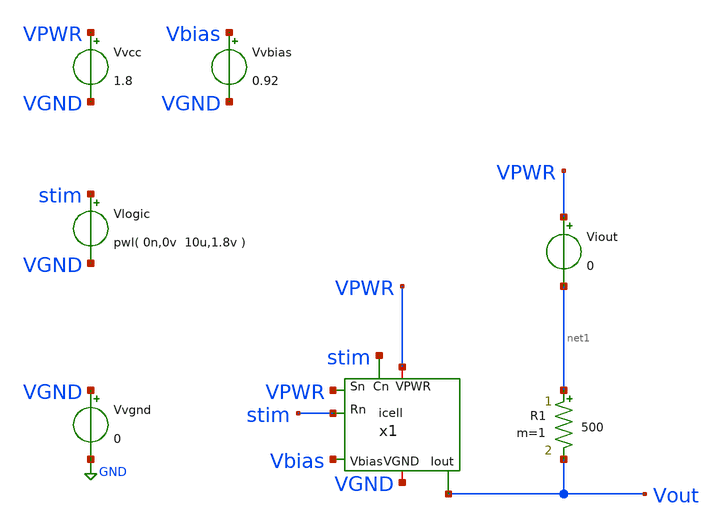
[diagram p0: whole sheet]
** sch_path: xschem/tb_icell.sch
**.subckt tb_icell
x1 VPWR VGND stim stim VPWR Vbias Vout icell
Vvcc VPWR VGND 1.8
R1 net1 Vout 500 m=1
Vvbias Vbias VGND 0.92
Vvgnd VGND GND 0
Viout VPWR net1 0
Vlogic stim VGND pwl( 0n,0v 10u,1.8v )
**** begin user architecture code



.options savecurrents
.control

    save all
    tran 1n 12.8u
    write tb_icell.raw vout

.endc




.lib $::SKYWATER_MODELS/sky130.lib.spice tt
.include $::SKYWATER_STDCELLS/sky130_fd_sc_hd.spice

**** end user architecture code
**.ends

* expanding   symbol:  icell.sym # of pins=7
** sym_path: xschem/icell.sym
** sch_path: xschem/icell.sch
.subckt icell VPWR VGND Rn Cn Sn Vbias Iout
*.ipin Rn
*.iopin VPWR
*.opin Iout
*.iopin VGND
*.ipin Cn
*.ipin Sn
*.ipin Vbias
XM2 net1 Sn VPWR VPWR sky130_fd_pr__pfet_01v8 L=0.15 W=0.5 nf=1 ad='int((nf+1)/2) * W/nf * 0.29' as='int((nf+2)/2) * W/nf * 0.29'
+ pd='2*int((nf+1)/2) * (W/nf + 0.29)' ps='2*int((nf+2)/2) * (W/nf + 0.29)' nrd='0.29 / W' nrs='0.29 / W'
+ sa=0 sb=0 sd=0 mult=1 m=1
XM3 net1 Sn net3 VGND sky130_fd_pr__nfet_01v8 L=0.15 W=0.5 nf=1 ad='int((nf+1)/2) * W/nf * 0.29' as='int((nf+2)/2) * W/nf * 0.29'
+ pd='2*int((nf+1)/2) * (W/nf + 0.29)' ps='2*int((nf+2)/2) * (W/nf + 0.29)' nrd='0.29 / W' nrs='0.29 / W'
+ sa=0 sb=0 sd=0 mult=1 m=1
XM4 net1 Cn net2 VPWR sky130_fd_pr__pfet_01v8 L=0.15 W=0.5 nf=1 ad='int((nf+1)/2) * W/nf * 0.29' as='int((nf+2)/2) * W/nf * 0.29'
+ pd='2*int((nf+1)/2) * (W/nf + 0.29)' ps='2*int((nf+2)/2) * (W/nf + 0.29)' nrd='0.29 / W' nrs='0.29 / W'
+ sa=0 sb=0 sd=0 mult=1 m=1
XM5 net2 Rn VPWR VPWR sky130_fd_pr__pfet_01v8 L=0.15 W=0.5 nf=1 ad='int((nf+1)/2) * W/nf * 0.29' as='int((nf+2)/2) * W/nf * 0.29'
+ pd='2*int((nf+1)/2) * (W/nf + 0.29)' ps='2*int((nf+2)/2) * (W/nf + 0.29)' nrd='0.29 / W' nrs='0.29 / W'
+ sa=0 sb=0 sd=0 mult=1 m=1
XM6 net3 Rn VGND VGND sky130_fd_pr__nfet_01v8 L=0.15 W=0.5 nf=1 ad='int((nf+1)/2) * W/nf * 0.29' as='int((nf+2)/2) * W/nf * 0.29'
+ pd='2*int((nf+1)/2) * (W/nf + 0.29)' ps='2*int((nf+2)/2) * (W/nf + 0.29)' nrd='0.29 / W' nrs='0.29 / W'
+ sa=0 sb=0 sd=0 mult=1 m=1
XM7 net3 Cn VGND VGND sky130_fd_pr__nfet_01v8 L=0.15 W=0.5 nf=1 ad='int((nf+1)/2) * W/nf * 0.29' as='int((nf+2)/2) * W/nf * 0.29'
+ pd='2*int((nf+1)/2) * (W/nf + 0.29)' ps='2*int((nf+2)/2) * (W/nf + 0.29)' nrd='0.29 / W' nrs='0.29 / W'
+ sa=0 sb=0 sd=0 mult=1 m=1
XM1 net4 Vbias VGND VGND sky130_fd_pr__nfet_g5v0d10v5 L=0.5 W=0.5 nf=1 ad='int((nf+1)/2) * W/nf * 0.29'
+ as='int((nf+2)/2) * W/nf * 0.29' pd='2*int((nf+1)/2) * (W/nf + 0.29)' ps='2*int((nf+2)/2) * (W/nf + 0.29)'
+ nrd='0.29 / W' nrs='0.29 / W' sa=0 sb=0 sd=0 mult=1 m=1
XM8 Iout net1 net4 VGND sky130_fd_pr__nfet_g5v0d10v5 L=0.5 W=1.0 nf=1 ad='int((nf+1)/2) * W/nf * 0.29'
+ as='int((nf+2)/2) * W/nf * 0.29' pd='2*int((nf+1)/2) * (W/nf + 0.29)' ps='2*int((nf+2)/2) * (W/nf + 0.29)'
+ nrd='0.29 / W' nrs='0.29 / W' sa=0 sb=0 sd=0 mult=1 m=1
.ends

.GLOBAL GND
.end
